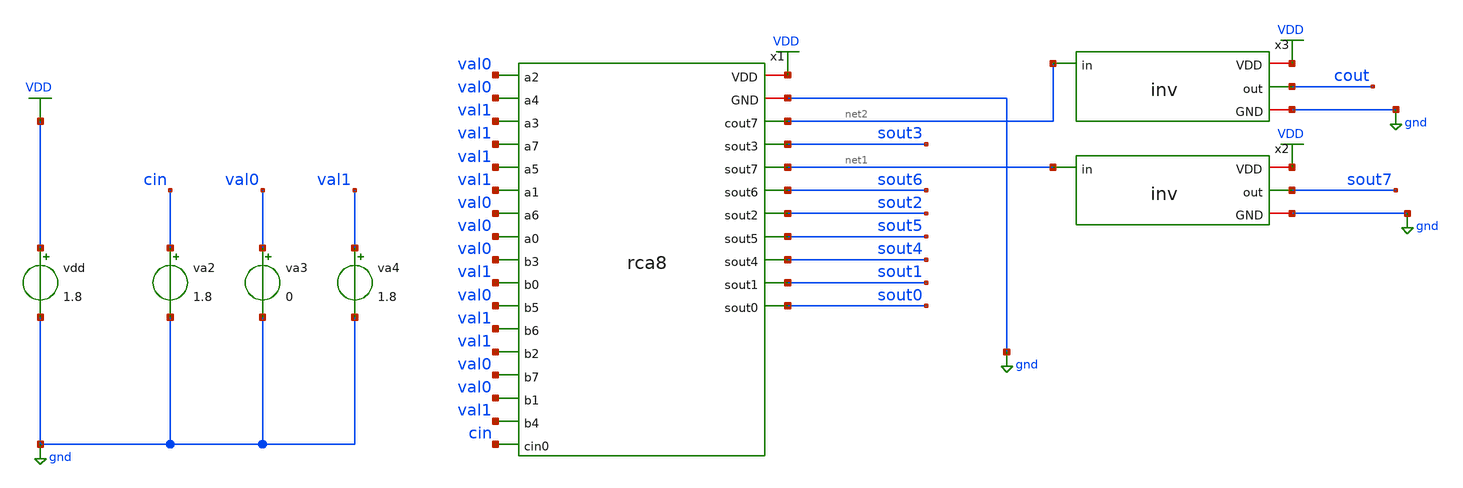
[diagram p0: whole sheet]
** sch_path: assignments/assignment8/assignrca1.sch
**.subckt assignrca1
x1 VDD gnd val0 val0 val1 val1 val1 val1 val0 val0 val0 val1 val0 val1 val1 val0 val0 val1 cin net2
+ sout3 net1 sout6 sout2 sout5 sout4 sout1 sout0 rca8
vdd VDD gnd 1.8
va3 val0 gnd 0
va4 val1 gnd 1.8
va2 cin gnd 1.8
x2 VDD net1 sout7 gnd inv
x3 VDD net2 cout gnd inv
**** begin user architecture code


*.include rca8_extracted.spice
.save all
.control
alter @va2[pulse] = [ 0 1.8 0 10p 10p 4n 8n ]
tran 5p 40n

* cin -> cout7 (adder output, before the load inverter x3)
meas tran c_delay_fall TRIG v(cin) VAL=0.9 RISE=3 TARG v(cout) VAL=0.9 FALL=3
meas tran c_delay_rise TRIG v(cin) VAL=0.9 FALL=3 TARG v(cout) VAL=0.9 RISE=3

* cin -> sum7 (adder output, before the output inverter x2)
meas tran s_delay_rise TRIG v(cin) VAL=0.9 RISE=3 TARG v(sout7) VAL=0.9 RISE=3
meas tran s_delay_fall TRIG v(cin) VAL=0.9 FALL=3 TARG v(sout7) VAL=0.9 FALL=3

let cin_to_cout=(c_delay_rise+c_delay_fall)/2
let cin_to_s7=(s_delay_rise+s_delay_fall)/2
print cin_to_cout cin_to_s7
plot v(cin) v(cout) v(sout7)
.endc


.lib $::SKYWATER_MODELS/sky130.lib.spice tt
**** end user architecture code
**.ends
.GLOBAL VDD
.GLOBAL gnd
.end
